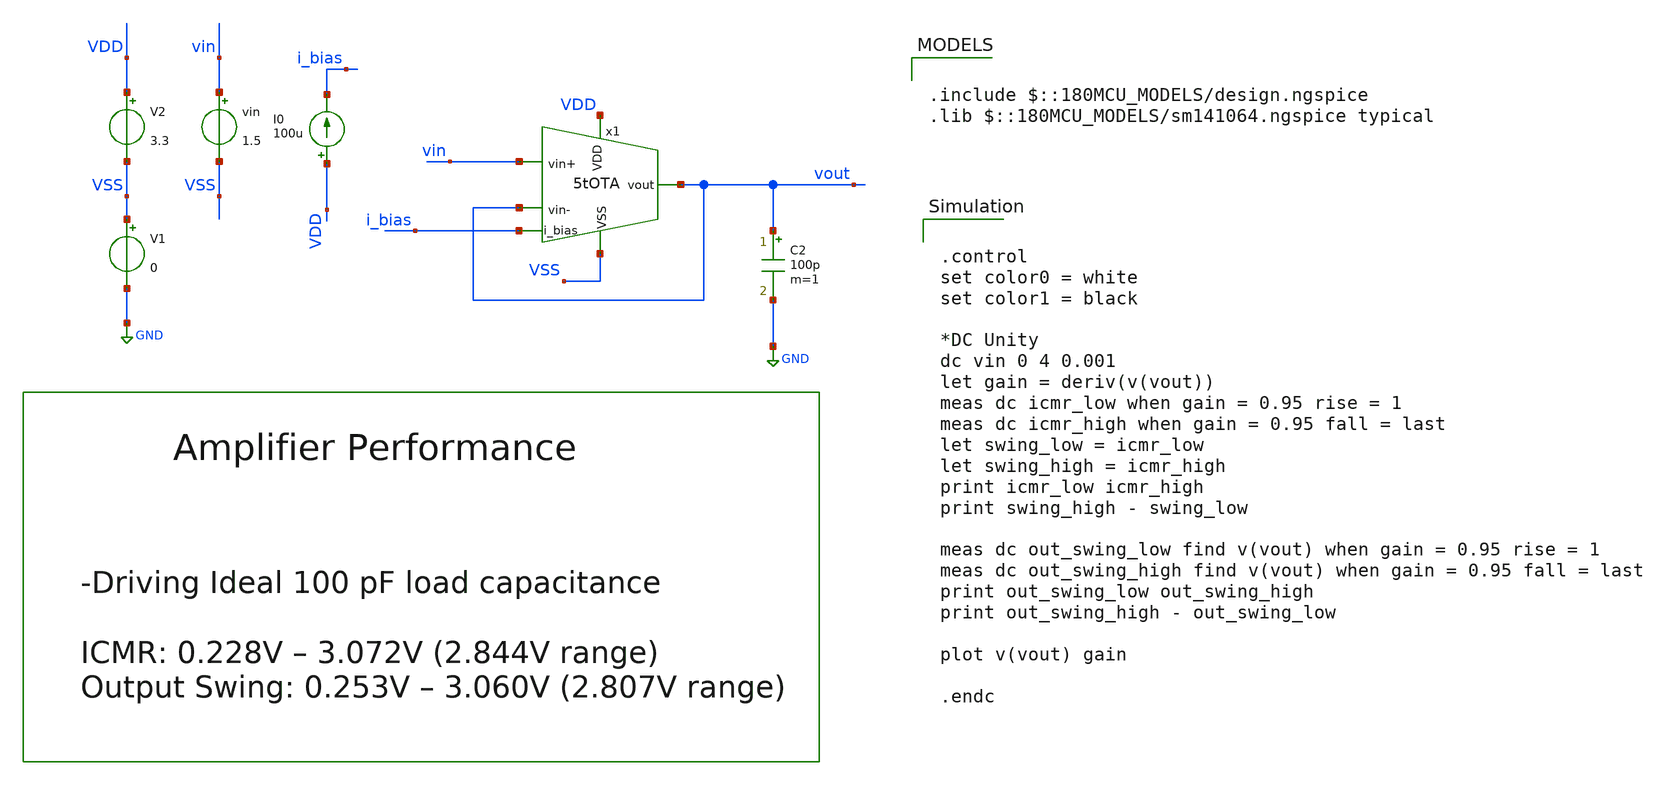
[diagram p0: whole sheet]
** sch_path: designs/libs/core_amps/ota_5t/tb/5tOTA_tb_dc.sch
**.subckt 5tOTA_tb_dc
V1 VSS GND 0
V2 VDD VSS 3.3
I0 VDD i_bias 100u
vin vin VSS 1.5
C2 vout GND 100p m=1
x1 VDD vout vin vout i_bias VSS 5tOTA
**** begin user architecture code

.include $::180MCU_MODELS/design.ngspice
.lib $::180MCU_MODELS/sm141064.ngspice typical



.control
set color0 = white
set color1 = black

*DC Unity
dc vin 0 4 0.001
let gain = deriv(v(vout))
meas dc icmr_low when gain = 0.95 rise = 1
meas dc icmr_high when gain = 0.95 fall = last
let swing_low = icmr_low
let swing_high = icmr_high
print icmr_low icmr_high
print swing_high - swing_low

meas dc out_swing_low find v(vout) when gain = 0.95 rise = 1
meas dc out_swing_high find v(vout) when gain = 0.95 fall = last
print out_swing_low out_swing_high
print out_swing_high - out_swing_low

plot v(vout) gain

.endc


**** end user architecture code
**.ends

* expanding   symbol:  libs/core_amps/ota_5t/schem/5tOTA.sym # of pins=6
** sym_path: designs/5tOTA.sym
** sch_path: designs/5tOTA.sch
.subckt 5tOTA VDD vout vin+ vin- i_bias VSS
*.ipin VDD
*.opin vout
*.ipin i_bias
*.ipin vin+
*.ipin vin-
*.ipin VSS
XM1 net1 vin+ net2 VSS nfet_03v3 L=0.5u W=11.43u nf=1 ad='int((nf+1)/2) * W/nf * 0.18u' as='int((nf+2)/2) * W/nf * 0.18u'
+ pd='2*int((nf+1)/2) * (W/nf + 0.18u)' ps='2*int((nf+2)/2) * (W/nf + 0.18u)' nrd='0.18u / W' nrs='0.18u / W'
+ sa=0 sb=0 sd=0 m=1
XM2 vout vin- net2 VSS nfet_03v3 L=0.5u W=11.43u nf=1 ad='int((nf+1)/2) * W/nf * 0.18u' as='int((nf+2)/2) * W/nf * 0.18u'
+ pd='2*int((nf+1)/2) * (W/nf + 0.18u)' ps='2*int((nf+2)/2) * (W/nf + 0.18u)' nrd='0.18u / W' nrs='0.18u / W'
+ sa=0 sb=0 sd=0 m=1
XM3 net1 net1 VDD VDD pfet_03v3 L=0.5u W=22.86u nf=1 ad='int((nf+1)/2) * W/nf * 0.18u' as='int((nf+2)/2) * W/nf * 0.18u'
+ pd='2*int((nf+1)/2) * (W/nf + 0.18u)' ps='2*int((nf+2)/2) * (W/nf + 0.18u)' nrd='0.18u / W' nrs='0.18u / W'
+ sa=0 sb=0 sd=0 m=1
XM4 vout net1 VDD VDD pfet_03v3 L=0.5u W=22.86u nf=1 ad='int((nf+1)/2) * W/nf * 0.18u' as='int((nf+2)/2) * W/nf * 0.18u'
+ pd='2*int((nf+1)/2) * (W/nf + 0.18u)' ps='2*int((nf+2)/2) * (W/nf + 0.18u)' nrd='0.18u / W' nrs='0.18u / W'
+ sa=0 sb=0 sd=0 m=1
XM5 net2 i_bias VSS VSS nfet_03v3 L=0.5u W=22.86u nf=1 ad='int((nf+1)/2) * W/nf * 0.18u' as='int((nf+2)/2) * W/nf * 0.18u'
+ pd='2*int((nf+1)/2) * (W/nf + 0.18u)' ps='2*int((nf+2)/2) * (W/nf + 0.18u)' nrd='0.18u / W' nrs='0.18u / W'
+ sa=0 sb=0 sd=0 m=1
XM6 i_bias i_bias VSS VSS nfet_03v3 L=0.5u W=22.86u nf=1 ad='int((nf+1)/2) * W/nf * 0.18u' as='int((nf+2)/2) * W/nf * 0.18u'
+ pd='2*int((nf+1)/2) * (W/nf + 0.18u)' ps='2*int((nf+2)/2) * (W/nf + 0.18u)' nrd='0.18u / W' nrs='0.18u / W'
+ sa=0 sb=0 sd=0 m=1
.ends

.GLOBAL GND
.end
